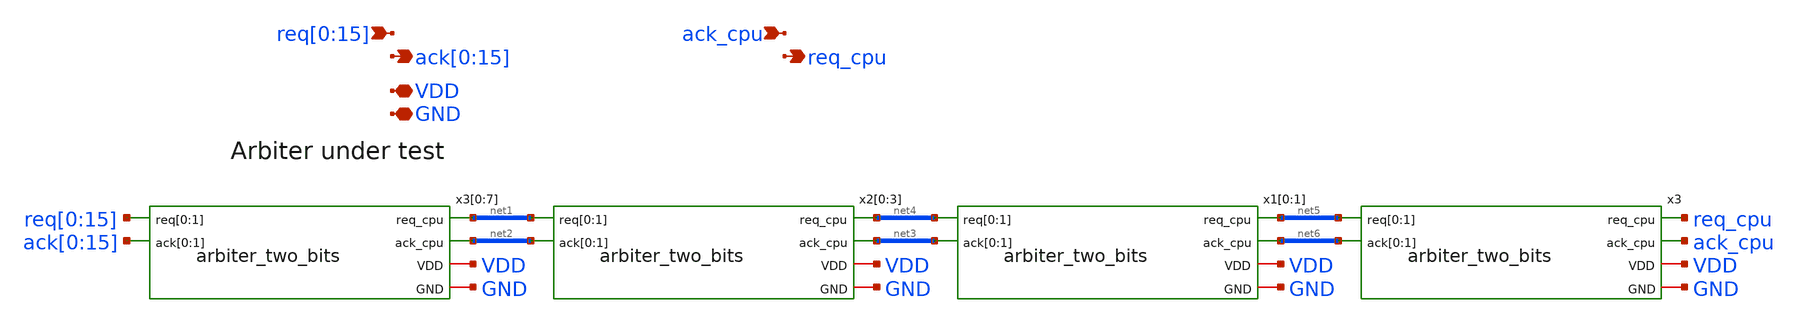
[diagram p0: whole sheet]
** sch_path: design/xschem/arbiter_tree_sixteen_bits.sch
**.subckt arbiter_tree_sixteen_bits
*+ req[0],req[1],req[2],req[3],req[4],req[5],req[6],req[7],req[8],req[9],req[10],req[11],req[12],req[13],req[14],req[15]
*+ ack[0],ack[1],ack[2],ack[3],ack[4],ack[5],ack[6],ack[7],ack[8],ack[9],ack[10],ack[11],ack[12],ack[13],ack[14],ack[15] ack_cpu req_cpu VDD GND
*.ipin
*+ req[0],req[1],req[2],req[3],req[4],req[5],req[6],req[7],req[8],req[9],req[10],req[11],req[12],req[13],req[14],req[15]
*.opin
*+ ack[0],ack[1],ack[2],ack[3],ack[4],ack[5],ack[6],ack[7],ack[8],ack[9],ack[10],ack[11],ack[12],ack[13],ack[14],ack[15]
*.ipin ack_cpu
*.opin req_cpu
*.iopin VDD
*.iopin GND
x3 net5[1] net5[0] ack_cpu net6[1] net6[0] req_cpu VDD GND arbiter_two_bits
x1[0] net4[3] net4[2] net6[1] net3[3] net3[2] net5[1] VDD GND arbiter_two_bits
x1[1] net4[1] net4[0] net6[0] net3[1] net3[0] net5[0] VDD GND arbiter_two_bits
x2[0] net1[7] net1[6] net3[3] net2[7] net2[6] net4[3] VDD GND arbiter_two_bits
x2[1] net1[5] net1[4] net3[2] net2[5] net2[4] net4[2] VDD GND arbiter_two_bits
x2[2] net1[3] net1[2] net3[1] net2[3] net2[2] net4[1] VDD GND arbiter_two_bits
x2[3] net1[1] net1[0] net3[0] net2[1] net2[0] net4[0] VDD GND arbiter_two_bits
x3[0] req[0] req[1] net2[7] ack[0] ack[1] net1[7] VDD GND arbiter_two_bits
x3[1] req[2] req[3] net2[6] ack[2] ack[3] net1[6] VDD GND arbiter_two_bits
x3[2] req[4] req[5] net2[5] ack[4] ack[5] net1[5] VDD GND arbiter_two_bits
x3[3] req[6] req[7] net2[4] ack[6] ack[7] net1[4] VDD GND arbiter_two_bits
x3[4] req[8] req[9] net2[3] ack[8] ack[9] net1[3] VDD GND arbiter_two_bits
x3[5] req[10] req[11] net2[2] ack[10] ack[11] net1[2] VDD GND arbiter_two_bits
x3[6] req[12] req[13] net2[1] ack[12] ack[13] net1[1] VDD GND arbiter_two_bits
x3[7] req[14] req[15] net2[0] ack[14] ack[15] net1[0] VDD GND arbiter_two_bits
**.ends

* expanding   symbol:  arbiter_two_bits.sym # of pins=6
** sym_path: design/xschem/arbiter_two_bits.sym
** sch_path: design/xschem/arbiter_two_bits.sch
.subckt arbiter_two_bits req[0] req[1] ack_cpu ack[0] ack[1] req_cpu VDD GND
*.ipin req[0],req[1]
*.opin ack[0],ack[1]
*.ipin ack_cpu
*.opin req_cpu
*.iopin VDD
*.iopin GND
x1 ack[1] ack[0] ack_cpu req_cpu req[0] req[1] VDD GND arbiter_cell_two_bits_fc
.ends


* expanding   symbol:  arbiter_cell_two_bits_fc.sym # of pins=8
** sym_path: design/xschem/arbiter_cell_two_bits_fc.sym
** sch_path: design/xschem/arbiter_cell_two_bits_fc.sch
.subckt arbiter_cell_two_bits_fc g1 g0 gc rc r0 r1 VDD GND
*.ipin r1
*.ipin r0
*.opin g0
*.opin g1
*.opin rc
*.ipin gc
*.iopin GND
*.iopin VDD
x1 net6 net5 GND GND VDD VDD net7 sky130_fd_sc_hd__nand2_1
x2 r0 gc GND GND VDD VDD net4 sky130_fd_sc_hd__or2_1
x3 net3 net1 GND GND VDD VDD g0 sky130_fd_sc_hd__nor2_1
x4 net6 net6 net6 net6 GND GND VDD VDD net3 sky130_fd_sc_hd__or4_1
x5 gc GND GND VDD VDD net1 sky130_fd_sc_hd__inv_1
x6 gc r1 GND GND VDD VDD net5 sky130_fd_sc_hd__or2_1
x7 net4 net7 GND GND VDD VDD net6 sky130_fd_sc_hd__nand2_1
x8 net7 net7 net7 net7 GND GND VDD VDD net2 sky130_fd_sc_hd__or4_1
x9 net1 net2 GND GND VDD VDD g1 sky130_fd_sc_hd__nor2_1
x10 net2 r0 GND GND VDD VDD net8 sky130_fd_sc_hd__nand2_1
x11 net3 r1 GND GND VDD VDD net9 sky130_fd_sc_hd__nand2_1
x12 net8 net9 GND GND VDD VDD rc sky130_fd_sc_hd__nand2_1
.ends

.end
